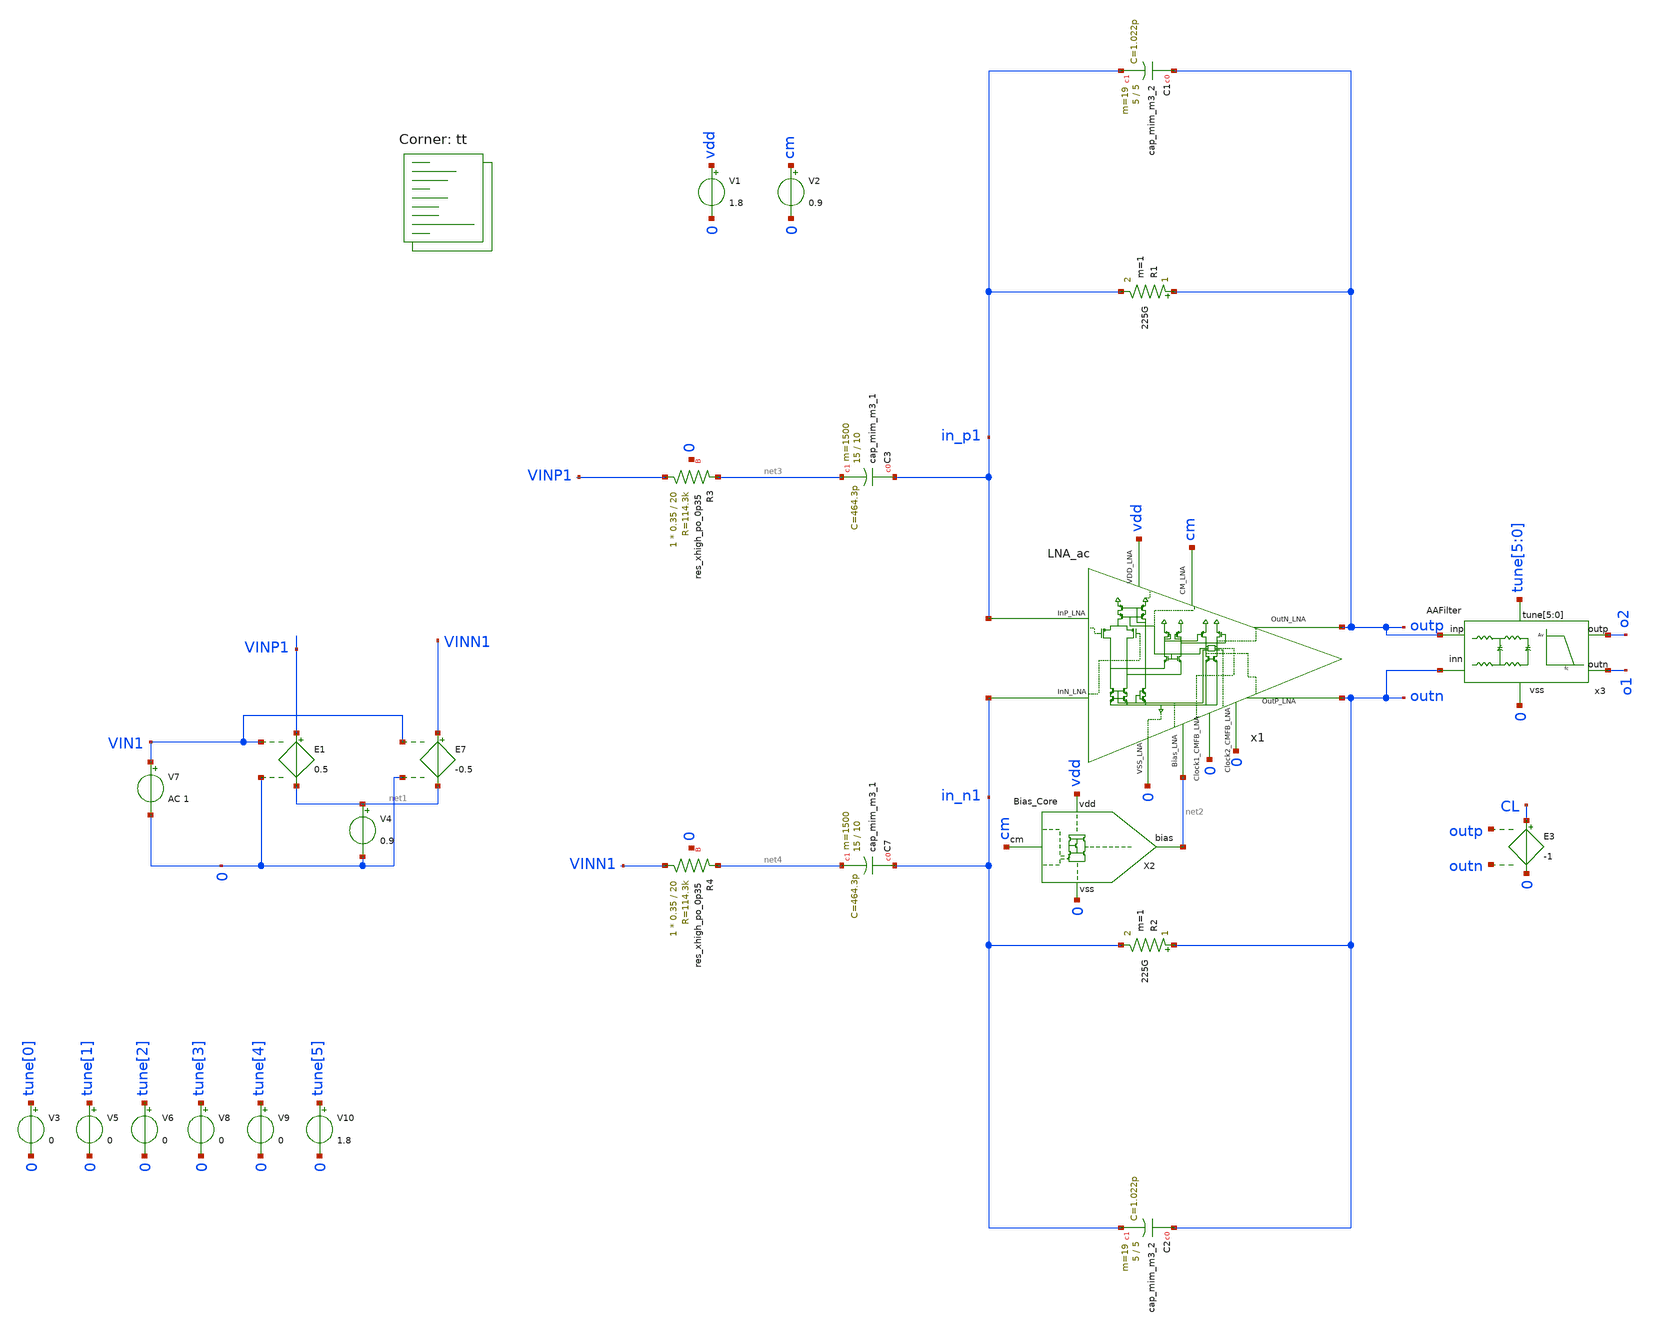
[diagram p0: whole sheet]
** sch_path: CL_ac.sch
**.subckt CL_ac
x1 in_n1 in_p1 vdd cm outp outn 0 net2 0 0 LNA_ac
V1 vdd 0 1.8
V2 cm 0 0.9
E1 VINP1 net1 VIN1 0 0.5
E7 VINN1 net1 VIN1 0 -0.5
V4 net1 0 0.9
V7 VIN1 0 AC 1
R1 outp in_p1 225G m=1
XC1 outp in_p1 sky130_fd_pr__cap_mim_m3_2 W=5 L=5 MF=19 m=19
XC2 outn in_n1 sky130_fd_pr__cap_mim_m3_2 W=5 L=5 MF=19 m=19
R2 outn in_n1 225G m=1
XR3 VINP1 net3 0 sky130_fd_pr__res_xhigh_po_0p35 L=20 mult=1 m=1
XR4 VINN1 net4 0 sky130_fd_pr__res_xhigh_po_0p35 L=20 mult=1 m=1
x3 outp outn o2 o1 0 tune[5] tune[4] tune[3] tune[2] tune[1] tune[0] AAFilter
X2 cm vdd 0 net2 Bias_Core
E3 CL 0 outp outn -1
V3 tune[0] 0 0
V5 tune[1] 0 0
V6 tune[2] 0 0
V8 tune[3] 0 0
V9 tune[4] 0 0
V10 tune[5] 0 1.8
XC7 in_n1 net4 sky130_fd_pr__cap_mim_m3_1 W=15 L=10 MF=1500 m=1500
XC3 in_p1 net3 sky130_fd_pr__cap_mim_m3_1 W=15 L=10 MF=1500 m=1500
**** begin user architecture code
.lib $::SKYWATER_MODELS/sky130.lib.spice tt


.options savecurrents gmin=1e-13
*ic v(VM5)=0.9 v(VM6)=0.9
.control


save all

save @m.xm11.msky130_fd_pr__pfet_01v8_lvt[id]
save @m.xm11.msky130_fd_pr__pfet_01v8_lvt[vgs]


*nmos
save @m.xm3.msky130_fd_pr__nfet_01v8_lvt[vgs]
save @m.xm3.msky130_fd_pr__nfet_01v8_lvt[vth]
save @m.xm3.msky130_fd_pr__nfet_01v8_lvt[vds]

save @m.xm6.msky130_fd_pr__nfet_01v8_lvt[vgs]
save @m.xm6.msky130_fd_pr__nfet_01v8_lvt[vth]
save @m.xm6.msky130_fd_pr__nfet_01v8_lvt[vds]

save @m.xm8.msky130_fd_pr__nfet_01v8_lvt[vgs]
save @m.xm8.msky130_fd_pr__nfet_01v8_lvt[vth]
save @m.xm8.msky130_fd_pr__nfet_01v8_lvt[vds]

save @m.xm9.msky130_fd_pr__nfet_01v8_lvt[vgs]
save @m.xm9.msky130_fd_pr__nfet_01v8_lvt[vth]
save @m.xm9.msky130_fd_pr__nfet_01v8_lvt[vds]

save @m.xm18.msky130_fd_pr__nfet_01v8_lvt[vgs]
save @m.xm18.msky130_fd_pr__nfet_01v8_lvt[vth]
save @m.xm18.msky130_fd_pr__nfet_01v8_lvt[vds]

save @m.xm19.msky130_fd_pr__nfet_01v8_lvt[vgs]
save @m.xm19.msky130_fd_pr__nfet_01v8_lvt[vth]
save @m.xm19.msky130_fd_pr__nfet_01v8_lvt[vds]

save @m.xm25.msky130_fd_pr__nfet_01v8_lvt[vgs]
save @m.xm25.msky130_fd_pr__nfet_01v8_lvt[vth]
save @m.xm25.msky130_fd_pr__nfet_01v8_lvt[vds]

*pmos

save @m.xm1.msky130_fd_pr__pfet_01v8_lvt[vgs]
save @m.xm1.msky130_fd_pr__pfet_01v8_lvt[vth]
save @m.xm1.msky130_fd_pr__pfet_01v8_lvt[vds]


save @m.xm2.msky130_fd_pr__pfet_01v8_lvt[vgs]
save @m.xm2.msky130_fd_pr__pfet_01v8_lvt[vth]
save @m.xm2.msky130_fd_pr__pfet_01v8_lvt[vds]


save @m.xm10.msky130_fd_pr__pfet_01v8_lvt[vgs]
save @m.xm10.msky130_fd_pr__pfet_01v8_lvt[vth]
save @m.xm10.msky130_fd_pr__pfet_01v8_lvt[vds]

save @m.xm13.msky130_fd_pr__pfet_01v8_lvt[vgs]
save @m.xm13.msky130_fd_pr__pfet_01v8_lvt[vth]
save @m.xm13.msky130_fd_pr__pfet_01v8_lvt[vds]

save @m.xm4.msky130_fd_pr__pfet_01v8_lvt[vgs]
save @m.xm4.msky130_fd_pr__pfet_01v8_lvt[vth]
save @m.xm4.msky130_fd_pr__pfet_01v8_lvt[vds]

save @m.xm5.msky130_fd_pr__pfet_01v8_lvt[vgs]
save @m.xm5.msky130_fd_pr__pfet_01v8_lvt[vth]
save @m.xm5.msky130_fd_pr__pfet_01v8_lvt[vds]

save @m.xm16.msky130_fd_pr__pfet_01v8_lvt[vgs]
save @m.xm16.msky130_fd_pr__pfet_01v8_lvt[vth]
save @m.xm16.msky130_fd_pr__pfet_01v8_lvt[vds]

save @m.xm17.msky130_fd_pr__pfet_01v8_lvt[vgs]
save @m.xm17.msky130_fd_pr__pfet_01v8_lvt[vth]
save @m.xm17.msky130_fd_pr__pfet_01v8_lvt[vds]

save @m.xm3.msky130_fd_pr__pfet_01v8_lvt[vgs]
save @m.xm3.msky130_fd_pr__pfet_01v8_lvt[vth]
save @m.xm3.msky130_fd_pr__pfet_01v8_lvt[vds]

save @m.xm20.msky130_fd_pr__pfet_01v8_lvt[vgs]
save @m.xm20.msky130_fd_pr__pfet_01v8_lvt[vth]
save @m.xm20.msky130_fd_pr__pfet_01v8_lvt[vds]

save @m.xm2.msky130_fd_pr__pfet_01v8_lvt[vgs]
save @m.xm2.msky130_fd_pr__pfet_01v8_lvt[vth]
save @m.xm2.msky130_fd_pr__pfet_01v8_lvt[vds]

save @m.xm21.msky130_fd_pr__pfet_01v8_lvt[vgs]
save @m.xm21.msky130_fd_pr__pfet_01v8_lvt[vth]
save @m.xm21.msky130_fd_pr__pfet_01v8_lvt[vds]

save @m.xm7.msky130_fd_pr__nfet_01v8_lvt[vth]

save @m.xm1.msky130_fd_pr__pfet_01v8[vgs]

save @m.xm1.msky130_fd_pr__nfet_01v8_lvt[gm]


save @m.xm1.msky130_fd_pr__nfet_01v8_lvt[gds]
save @m.xm2.msky130_fd_pr__pfet_01v8_lvt[gm]

save @m.xm23.msky130_fd_pr__nfet_01v8[cgs]
save @m.xm4.msky130_fd_pr__pfet_01v8[cgs]
save @m.xm2.msky130_fd_pr__pfet_01v8_lvt[cgs]



save @m.xm2.msky130_fd_pr__pfet_01v8_lvt[gds]


op
write CL_ac.raw
*set appendwrite


.endc
.control



*tran 50u 1500m
*save all
*plot v(Outp)-v(outn)


noise V(Outp,Outn) V7 dec 100 0.1 128
print inoise_total onoise_total
setplot noise1
plot inoise_spectrum

ac dec 10 0.1 10k
let gaind=(v(outp)-v(outn))/(v(VINP1)-v(VINN1))
let lg=vr/VIN1
let BG=(OL/CL)-1
let phase=180*cph(BG)/pi
plot db(gaind)
plot db(BG) phase


.endc






.include $::SKYWATER_STDCELLS/sky130_fd_sc_hd.spice

**** end user architecture code
**.ends

* expanding   symbol:  LNA/LNA_ac.sym # of pins=10
** sym_path: LNA_ac.sym
** sch_path: LNA_ac.sch
.subckt LNA_ac InN_LNA InP_LNA VDD_LNA CM_LNA OutN_LNA OutP_LNA VSS_LNA Bias_LNA Clock1_CMFB_LNA
+ Clock2_CMFB_LNA
*.iopin InP_LNA
*.iopin InN_LNA
*.iopin VSS_LNA
*.iopin VDD_LNA
*.iopin CM_LNA
*.opin OutP_LNA
*.opin OutN_LNA
*.iopin Clock2_CMFB_LNA
*.iopin Bias_LNA
*.iopin Clock1_CMFB_LNA
XM4 net4 InP_LNA VT2 VT2 sky130_fd_pr__pfet_01v8_lvt L=10 W=90 nf=1 ad='int((nf+1)/2) * W/nf * 0.29'
+ as='int((nf+2)/2) * W/nf * 0.29' pd='2*int((nf+1)/2) * (W/nf + 0.29)' ps='2*int((nf+2)/2) * (W/nf + 0.29)'
+ nrd='0.29 / W' nrs='0.29 / W' sa=0 sb=0 sd=0 mult=5 m=5
XM5 net3 InN_LNA VT2 VT2 sky130_fd_pr__pfet_01v8_lvt L=10 W=90 nf=1 ad='int((nf+1)/2) * W/nf * 0.29'
+ as='int((nf+2)/2) * W/nf * 0.29' pd='2*int((nf+1)/2) * (W/nf + 0.29)' ps='2*int((nf+2)/2) * (W/nf + 0.29)'
+ nrd='0.29 / W' nrs='0.29 / W' sa=0 sb=0 sd=0 mult=5 m=5
XM8 net8 Bias_LNA VSS_LNA VSS_LNA sky130_fd_pr__nfet_01v8_lvt L=20 W=10 nf=1 ad='int((nf+1)/2) * W/nf * 0.29'
+ as='int((nf+2)/2) * W/nf * 0.29' pd='2*int((nf+1)/2) * (W/nf + 0.29)' ps='2*int((nf+2)/2) * (W/nf + 0.29)'
+ nrd='0.29 / W' nrs='0.29 / W' sa=0 sb=0 sd=0 mult=3 m=3
XM9 net9 Bias_LNA VSS_LNA VSS_LNA sky130_fd_pr__nfet_01v8_lvt L=20 W=10 nf=1 ad='int((nf+1)/2) * W/nf * 0.29'
+ as='int((nf+2)/2) * W/nf * 0.29' pd='2*int((nf+1)/2) * (W/nf + 0.29)' ps='2*int((nf+2)/2) * (W/nf + 0.29)'
+ nrd='0.29 / W' nrs='0.29 / W' sa=0 sb=0 sd=0 mult=3 m=3
XM16 net7 b VDD_LNA VDD_LNA sky130_fd_pr__pfet_01v8_lvt L=20 W=6 nf=1 ad='int((nf+1)/2) * W/nf * 0.29'
+ as='int((nf+2)/2) * W/nf * 0.29' pd='2*int((nf+1)/2) * (W/nf + 0.29)' ps='2*int((nf+2)/2) * (W/nf + 0.29)'
+ nrd='0.29 / W' nrs='0.29 / W' sa=0 sb=0 sd=0 mult=1 m=1
XM17 net6 a VDD_LNA VDD_LNA sky130_fd_pr__pfet_01v8_lvt L=20 W=6 nf=1 ad='int((nf+1)/2) * W/nf * 0.29'
+ as='int((nf+2)/2) * W/nf * 0.29' pd='2*int((nf+1)/2) * (W/nf + 0.29)' ps='2*int((nf+2)/2) * (W/nf + 0.29)'
+ nrd='0.29 / W' nrs='0.29 / W' sa=0 sb=0 sd=0 mult=1 m=1
XM18 b CM_LNA net3 VSS_LNA sky130_fd_pr__nfet_01v8_lvt L=20 W=1 nf=1 ad='int((nf+1)/2) * W/nf * 0.29'
+ as='int((nf+2)/2) * W/nf * 0.29' pd='2*int((nf+1)/2) * (W/nf + 0.29)' ps='2*int((nf+2)/2) * (W/nf + 0.29)'
+ nrd='0.29 / W' nrs='0.29 / W' sa=0 sb=0 sd=0 mult=12 m=12
XM19 a CM_LNA net4 VSS_LNA sky130_fd_pr__nfet_01v8_lvt L=20 W=1 nf=1 ad='int((nf+1)/2) * W/nf * 0.29'
+ as='int((nf+2)/2) * W/nf * 0.29' pd='2*int((nf+1)/2) * (W/nf + 0.29)' ps='2*int((nf+2)/2) * (W/nf + 0.29)'
+ nrd='0.29 / W' nrs='0.29 / W' sa=0 sb=0 sd=0 mult=12 m=12
XM20 OutP_LNA a VDD_LNA VDD_LNA sky130_fd_pr__pfet_01v8_lvt L=20 W=6 nf=1 ad='int((nf+1)/2) * W/nf * 0.29'
+ as='int((nf+2)/2) * W/nf * 0.29' pd='2*int((nf+1)/2) * (W/nf + 0.29)' ps='2*int((nf+2)/2) * (W/nf + 0.29)'
+ nrd='0.29 / W' nrs='0.29 / W' sa=0 sb=0 sd=0 mult=10 m=10
XM21 OutN_LNA b VDD_LNA VDD_LNA sky130_fd_pr__pfet_01v8_lvt L=20 W=6 nf=1 ad='int((nf+1)/2) * W/nf * 0.29'
+ as='int((nf+2)/2) * W/nf * 0.29' pd='2*int((nf+1)/2) * (W/nf + 0.29)' ps='2*int((nf+2)/2) * (W/nf + 0.29)'
+ nrd='0.29 / W' nrs='0.29 / W' sa=0 sb=0 sd=0 mult=10 m=10
XM23 OutN_LNA net5 VSS_LNA VSS_LNA sky130_fd_pr__nfet_01v8_lvt L=20 W=10 nf=1 ad='int((nf+1)/2) * W/nf * 0.29'
+ as='int((nf+2)/2) * W/nf * 0.29' pd='2*int((nf+1)/2) * (W/nf + 0.29)' ps='2*int((nf+2)/2) * (W/nf + 0.29)'
+ nrd='0.29 / W' nrs='0.29 / W' sa=0 sb=0 sd=0 mult=10 m=10
XM25 OutP_LNA net5 VSS_LNA VSS_LNA sky130_fd_pr__nfet_01v8_lvt L=20 W=10 nf=1 ad='int((nf+1)/2) * W/nf * 0.29'
+ as='int((nf+2)/2) * W/nf * 0.29' pd='2*int((nf+1)/2) * (W/nf + 0.29)' ps='2*int((nf+2)/2) * (W/nf + 0.29)'
+ nrd='0.29 / W' nrs='0.29 / W' sa=0 sb=0 sd=0 mult=10 m=10
XM2 net10 net1 VDD_LNA VDD_LNA sky130_fd_pr__pfet_01v8_lvt L=20 W=2 nf=1 ad='int((nf+1)/2) * W/nf * 0.29'
+ as='int((nf+2)/2) * W/nf * 0.29' pd='2*int((nf+1)/2) * (W/nf + 0.29)' ps='2*int((nf+2)/2) * (W/nf + 0.29)'
+ nrd='0.29 / W' nrs='0.29 / W' sa=0 sb=0 sd=0 mult=4 m=4
XM3 net11 net1 VDD_LNA VDD_LNA sky130_fd_pr__pfet_01v8_lvt L=20 W=2 nf=1 ad='int((nf+1)/2) * W/nf * 0.29'
+ as='int((nf+2)/2) * W/nf * 0.29' pd='2*int((nf+1)/2) * (W/nf + 0.29)' ps='2*int((nf+2)/2) * (W/nf + 0.29)'
+ nrd='0.29 / W' nrs='0.29 / W' sa=0 sb=0 sd=0 mult=1 m=1
XM6 net2 Bias_LNA VSS_LNA VSS_LNA sky130_fd_pr__nfet_01v8_lvt L=20 W=10 nf=1 ad='int((nf+1)/2) * W/nf * 0.29'
+ as='int((nf+2)/2) * W/nf * 0.29' pd='2*int((nf+1)/2) * (W/nf + 0.29)' ps='2*int((nf+2)/2) * (W/nf + 0.29)'
+ nrd='0.29 / W' nrs='0.29 / W' sa=0 sb=0 sd=0 mult=1 m=1
E3 f1 VSS_LNA OutN_LNA VSS_LNA -1
E4 f2 VSS_LNA OutP_LNA f1 1
E5 f3 VSS_LNA f2 VSS_LNA 0.5
E6 net5 VSS_LNA CM_LNA f3 {-1000}
XC1 OutP_LNA a sky130_fd_pr__cap_mim_m3_2 W=12 L=10 MF=32 m=32
XC2 OutN_LNA b sky130_fd_pr__cap_mim_m3_2 W=12 L=10 MF=32 m=32
XM1 net4 CM_LNA net8 VSS_LNA sky130_fd_pr__nfet_01v8_lvt L=1 W=10 nf=1 ad='int((nf+1)/2) * W/nf * 0.29'
+ as='int((nf+2)/2) * W/nf * 0.29' pd='2*int((nf+1)/2) * (W/nf + 0.29)' ps='2*int((nf+2)/2) * (W/nf + 0.29)'
+ nrd='0.29 / W' nrs='0.29 / W' sa=0 sb=0 sd=0 mult=120 m=120
XM7 net3 CM_LNA net9 VSS_LNA sky130_fd_pr__nfet_01v8_lvt L=1 W=10 nf=1 ad='int((nf+1)/2) * W/nf * 0.29'
+ as='int((nf+2)/2) * W/nf * 0.29' pd='2*int((nf+1)/2) * (W/nf + 0.29)' ps='2*int((nf+2)/2) * (W/nf + 0.29)'
+ nrd='0.29 / W' nrs='0.29 / W' sa=0 sb=0 sd=0 mult=120 m=120
XM10 net1 CM_LNA net2 VSS_LNA sky130_fd_pr__nfet_01v8_lvt L=1 W=10 nf=1 ad='int((nf+1)/2) * W/nf * 0.29'
+ as='int((nf+2)/2) * W/nf * 0.29' pd='2*int((nf+1)/2) * (W/nf + 0.29)' ps='2*int((nf+2)/2) * (W/nf + 0.29)'
+ nrd='0.29 / W' nrs='0.29 / W' sa=0 sb=0 sd=0 mult=40 m=40
XM11 net1 CM_LNA net11 VDD_LNA sky130_fd_pr__pfet_01v8_lvt L=20 W=2 nf=1 ad='int((nf+1)/2) * W/nf * 0.29'
+ as='int((nf+2)/2) * W/nf * 0.29' pd='2*int((nf+1)/2) * (W/nf + 0.29)' ps='2*int((nf+2)/2) * (W/nf + 0.29)'
+ nrd='0.29 / W' nrs='0.29 / W' sa=0 sb=0 sd=0 mult=50 m=50
XM12 VT2 CM_LNA net10 VDD_LNA sky130_fd_pr__pfet_01v8_lvt L=20 W=2 nf=1 ad='int((nf+1)/2) * W/nf * 0.29'
+ as='int((nf+2)/2) * W/nf * 0.29' pd='2*int((nf+1)/2) * (W/nf + 0.29)' ps='2*int((nf+2)/2) * (W/nf + 0.29)'
+ nrd='0.29 / W' nrs='0.29 / W' sa=0 sb=0 sd=0 mult=200 m=200
XM13 b CM_LNA net7 VDD_LNA sky130_fd_pr__pfet_01v8_lvt L=20 W=6 nf=1 ad='int((nf+1)/2) * W/nf * 0.29'
+ as='int((nf+2)/2) * W/nf * 0.29' pd='2*int((nf+1)/2) * (W/nf + 0.29)' ps='2*int((nf+2)/2) * (W/nf + 0.29)'
+ nrd='0.29 / W' nrs='0.29 / W' sa=0 sb=0 sd=0 mult=10 m=10
XM14 a CM_LNA net6 VDD_LNA sky130_fd_pr__pfet_01v8_lvt L=20 W=6 nf=1 ad='int((nf+1)/2) * W/nf * 0.29'
+ as='int((nf+2)/2) * W/nf * 0.29' pd='2*int((nf+1)/2) * (W/nf + 0.29)' ps='2*int((nf+2)/2) * (W/nf + 0.29)'
+ nrd='0.29 / W' nrs='0.29 / W' sa=0 sb=0 sd=0 mult=10 m=10
.ends


* expanding   symbol:  LNA/AAFilter.sym # of pins=6
** sym_path: AAFilter.sym
** sch_path: AAFilter.sch
.subckt AAFilter inp inn outp outn vss tune[5] tune[4] tune[3] tune[2] tune[1] tune[0]
*.iopin inp
*.iopin inn
*.iopin vss
*.opin outp
*.opin outn
*.iopin tune[5],tune[4],tune[3],tune[2],tune[1],tune[0]
XR4 inp net3 vss sky130_fd_pr__res_xhigh_po_0p35 L=95 mult=1 m=1
XR15 net3 net1 vss sky130_fd_pr__res_xhigh_po_0p35 L=95 mult=1 m=1
XR16 net1 net4 vss sky130_fd_pr__res_xhigh_po_0p35 L=95 mult=1 m=1
XR17 net4 outp vss sky130_fd_pr__res_xhigh_po_0p35 L=95 mult=1 m=1
XR19 net2 net5 vss sky130_fd_pr__res_xhigh_po_0p35 L=95 mult=1 m=1
XR20 net5 inn vss sky130_fd_pr__res_xhigh_po_0p35 L=95 mult=1 m=1
XR23 outn net6 vss sky130_fd_pr__res_xhigh_po_0p35 L=95 mult=1 m=1
XR24 net6 net2 vss sky130_fd_pr__res_xhigh_po_0p35 L=95 mult=1 m=1
x2 outp outn vss tune[5] tune[4] tune[3] tune[2] tune[1] tune[0] capbank
x3 net1 net2 vss tune[5] tune[4] tune[3] tune[2] tune[1] tune[0] capbank
.ends


* expanding   symbol:  LNA/Bias_Core.sym # of pins=4
** sym_path: Bias_Core.sym
** sch_path: Bias_Core.sch
.subckt Bias_Core cm vdd vss bias
*.ipin vdd
*.ipin vss
*.opin bias
*.ipin cm
XM7 net3 bias vss vss sky130_fd_pr__nfet_01v8_lvt L=20 W=10 nf=1 ad='int((nf+1)/2) * W/nf * 0.29' as='int((nf+2)/2) * W/nf * 0.29'
+ pd='2*int((nf+1)/2) * (W/nf + 0.29)' ps='2*int((nf+2)/2) * (W/nf + 0.29)' nrd='0.29 / W' nrs='0.29 / W'
+ sa=0 sb=0 sd=0 mult=1 m=1
XM10 net4 vx vr vdd sky130_fd_pr__pfet_01v8_lvt L=20 W=10 nf=1 ad='int((nf+1)/2) * W/nf * 0.29' as='int((nf+2)/2) * W/nf * 0.29'
+ pd='2*int((nf+1)/2) * (W/nf + 0.29)' ps='2*int((nf+2)/2) * (W/nf + 0.29)' nrd='0.29 / W' nrs='0.29 / W'
+ sa=0 sb=0 sd=0 mult=20 m=20
XM11 bias cm net3 vss sky130_fd_pr__nfet_01v8_lvt L=20 W=10 nf=1 ad='int((nf+1)/2) * W/nf * 0.29' as='int((nf+2)/2) * W/nf * 0.29'
+ pd='2*int((nf+1)/2) * (W/nf + 0.29)' ps='2*int((nf+2)/2) * (W/nf + 0.29)' nrd='0.29 / W' nrs='0.29 / W'
+ sa=0 sb=0 sd=0 mult=40 m=40
XM12 net2 bias vss vss sky130_fd_pr__nfet_01v8_lvt L=20 W=10 nf=1 ad='int((nf+1)/2) * W/nf * 0.29' as='int((nf+2)/2) * W/nf * 0.29'
+ pd='2*int((nf+1)/2) * (W/nf + 0.29)' ps='2*int((nf+2)/2) * (W/nf + 0.29)' nrd='0.29 / W' nrs='0.29 / W'
+ sa=0 sb=0 sd=0 mult=1 m=1
XM13 vx cm net2 vss sky130_fd_pr__nfet_01v8_lvt L=20 W=10 nf=1 ad='int((nf+1)/2) * W/nf * 0.29' as='int((nf+2)/2) * W/nf * 0.29'
+ pd='2*int((nf+1)/2) * (W/nf + 0.29)' ps='2*int((nf+2)/2) * (W/nf + 0.29)' nrd='0.29 / W' nrs='0.29 / W'
+ sa=0 sb=0 sd=0 mult=40 m=40
XM2 net8 vx net1 vdd sky130_fd_pr__pfet_01v8_lvt L=20 W=10 nf=1 ad='int((nf+1)/2) * W/nf * 0.29' as='int((nf+2)/2) * W/nf * 0.29'
+ pd='2*int((nf+1)/2) * (W/nf + 0.29)' ps='2*int((nf+2)/2) * (W/nf + 0.29)' nrd='0.29 / W' nrs='0.29 / W'
+ sa=0 sb=0 sd=0 mult=20 m=20
XM3 net1 net1 vdd vdd sky130_fd_pr__pfet_01v8_lvt L=1 W=10 nf=1 ad='int((nf+1)/2) * W/nf * 0.29' as='int((nf+2)/2) * W/nf * 0.29'
+ pd='2*int((nf+1)/2) * (W/nf + 0.29)' ps='2*int((nf+2)/2) * (W/nf + 0.29)' nrd='0.29 / W' nrs='0.29 / W'
+ sa=0 sb=0 sd=0 mult=6 m=6
XM4 net5 net5 bias vss sky130_fd_pr__nfet_01v8_lvt L=10 W=1 nf=1 ad='int((nf+1)/2) * W/nf * 0.29' as='int((nf+2)/2) * W/nf * 0.29'
+ pd='2*int((nf+1)/2) * (W/nf + 0.29)' ps='2*int((nf+2)/2) * (W/nf + 0.29)' nrd='0.29 / W' nrs='0.29 / W'
+ sa=0 sb=0 sd=0 mult=1 m=1
XM5 net6 net6 net5 vss sky130_fd_pr__nfet_01v8_lvt L=10 W=1 nf=1 ad='int((nf+1)/2) * W/nf * 0.29' as='int((nf+2)/2) * W/nf * 0.29'
+ pd='2*int((nf+1)/2) * (W/nf + 0.29)' ps='2*int((nf+2)/2) * (W/nf + 0.29)' nrd='0.29 / W' nrs='0.29 / W'
+ sa=0 sb=0 sd=0 mult=1 m=1
XM8 net7 net7 net6 vss sky130_fd_pr__nfet_01v8_lvt L=10 W=1 nf=1 ad='int((nf+1)/2) * W/nf * 0.29' as='int((nf+2)/2) * W/nf * 0.29'
+ pd='2*int((nf+1)/2) * (W/nf + 0.29)' ps='2*int((nf+2)/2) * (W/nf + 0.29)' nrd='0.29 / W' nrs='0.29 / W'
+ sa=0 sb=0 sd=0 mult=1 m=1
XM9 vx vx net7 vss sky130_fd_pr__nfet_01v8_lvt L=10 W=1 nf=1 ad='int((nf+1)/2) * W/nf * 0.29' as='int((nf+2)/2) * W/nf * 0.29'
+ pd='2*int((nf+1)/2) * (W/nf + 0.29)' ps='2*int((nf+2)/2) * (W/nf + 0.29)' nrd='0.29 / W' nrs='0.29 / W'
+ sa=0 sb=0 sd=0 mult=1 m=1
XM23 bias vx net4 vdd sky130_fd_pr__pfet_01v8_lvt L=20 W=10 nf=1 ad='int((nf+1)/2) * W/nf * 0.29' as='int((nf+2)/2) * W/nf * 0.29'
+ pd='2*int((nf+1)/2) * (W/nf + 0.29)' ps='2*int((nf+2)/2) * (W/nf + 0.29)' nrd='0.29 / W' nrs='0.29 / W'
+ sa=0 sb=0 sd=0 mult=5 m=5
XM24 vx vx net8 vdd sky130_fd_pr__pfet_01v8_lvt L=20 W=10 nf=1 ad='int((nf+1)/2) * W/nf * 0.29' as='int((nf+2)/2) * W/nf * 0.29'
+ pd='2*int((nf+1)/2) * (W/nf + 0.29)' ps='2*int((nf+2)/2) * (W/nf + 0.29)' nrd='0.29 / W' nrs='0.29 / W'
+ sa=0 sb=0 sd=0 mult=5 m=5
R27 vdd vr 3e6 m=1
.ends


* expanding   symbol:  LNA/capbank.sym # of pins=4
** sym_path: capbank.sym
** sch_path: capbank.sch
.subckt capbank vp_cap vn_cap vss_cap tune[5] tune[4] tune[3] tune[2] tune[1] tune[0]
*.iopin vp_cap
*.iopin vn_cap
*.ipin tune[5],tune[4],tune[3],tune[2],tune[1],tune[0]
*.ipin vss_cap
x6 tune[5] net1 net2 vss_cap cap_sw
XC11 net2 vp_cap sky130_fd_pr__cap_mim_m3_1 W=5 L=5.5 MF=160 m=160
XC12 net1 vn_cap sky130_fd_pr__cap_mim_m3_1 W=5 L=5.5 MF=160 m=160
XC21 vn_cap net1 sky130_fd_pr__cap_mim_m3_1 W=5 L=5.5 MF=160 m=160
XC22 vp_cap net2 sky130_fd_pr__cap_mim_m3_1 W=5 L=5.5 MF=160 m=160
x1 tune[4] net3 net4 vss_cap cap_sw
XC1 net4 vp_cap sky130_fd_pr__cap_mim_m3_1 W=5 L=5.5 MF=80 m=80
XC2 net3 vn_cap sky130_fd_pr__cap_mim_m3_1 W=5 L=5.5 MF=80 m=80
XC3 vn_cap net3 sky130_fd_pr__cap_mim_m3_1 W=5 L=5.5 MF=80 m=80
XC4 vp_cap net4 sky130_fd_pr__cap_mim_m3_1 W=5 L=5.5 MF=80 m=80
x2 tune[3] net5 net6 vss_cap cap_sw
XC5 net6 vp_cap sky130_fd_pr__cap_mim_m3_1 W=5 L=5.5 MF=40 m=40
XC6 net5 vn_cap sky130_fd_pr__cap_mim_m3_1 W=5 L=5.5 MF=40 m=40
XC7 vn_cap net5 sky130_fd_pr__cap_mim_m3_1 W=5 L=5.5 MF=40 m=40
XC8 vp_cap net6 sky130_fd_pr__cap_mim_m3_1 W=5 L=5.5 MF=40 m=40
x3 tune[2] net7 net8 vss_cap cap_sw
XC9 net8 vp_cap sky130_fd_pr__cap_mim_m3_1 W=5 L=5.5 MF=20 m=20
XC10 net7 vn_cap sky130_fd_pr__cap_mim_m3_1 W=5 L=5.5 MF=20 m=20
XC13 vn_cap net7 sky130_fd_pr__cap_mim_m3_1 W=5 L=5.5 MF=20 m=20
XC14 vp_cap net8 sky130_fd_pr__cap_mim_m3_1 W=5 L=5.5 MF=20 m=20
x4 tune[1] net9 net10 vss_cap cap_sw
XC15 net10 vp_cap sky130_fd_pr__cap_mim_m3_1 W=5 L=5.5 MF=10 m=10
XC16 net9 vn_cap sky130_fd_pr__cap_mim_m3_1 W=5 L=5.5 MF=10 m=10
XC17 vn_cap net9 sky130_fd_pr__cap_mim_m3_1 W=5 L=5.5 MF=10 m=10
XC18 vp_cap net10 sky130_fd_pr__cap_mim_m3_1 W=5 L=5.5 MF=10 m=10
x5 tune[0] net11 net12 vss_cap cap_sw
XC19 vp_cap net12 sky130_fd_pr__cap_mim_m3_1 W=5 L=5.5 MF=5 m=5
XC20 vn_cap net11 sky130_fd_pr__cap_mim_m3_1 W=5 L=5.5 MF=5 m=5
XC23 vn_cap net11 sky130_fd_pr__cap_mim_m3_1 W=5 L=5.5 MF=5 m=5
XC24 vp_cap net12 sky130_fd_pr__cap_mim_m3_1 W=5 L=5.5 MF=5 m=5
.ends


* expanding   symbol:  LNA/cap_sw.sym # of pins=4
** sym_path: cap_sw.sym
** sch_path: cap_sw.sch
.subckt cap_sw en_sw vn_sw vp_sw vss_sw
*.ipin en_sw
*.ipin vss_sw
*.opin vn_sw
*.opin vp_sw
XM15 vp_sw en_sw vn_sw vss_sw sky130_fd_pr__nfet_01v8 L=0.15 W='5 * 13 ' nf=13 ad='int((nf+1)/2) * W / nf * 0.29'
+ as='int((nf+2)/2) * W / nf * 0.29' pd='2*int((nf+1)/2) * (W / nf + 0.29)' ps='2*int((nf+2)/2) * (W / nf + 0.29)'
+ nrd='0.29 / W ' nrs='0.29 / W ' sa=0 sb=0 sd=0 mult=1 m=1
XM5 vn_sw en_sw vss_sw vss_sw sky130_fd_pr__nfet_01v8 L=0.15 W='5 * 1 ' nf=1 ad='int((nf+1)/2) * W / nf * 0.29'
+ as='int((nf+2)/2) * W / nf * 0.29' pd='2*int((nf+1)/2) * (W / nf + 0.29)' ps='2*int((nf+2)/2) * (W / nf + 0.29)'
+ nrd='0.29 / W ' nrs='0.29 / W ' sa=0 sb=0 sd=0 mult=1 m=1
XM7 vp_sw en_sw vss_sw vss_sw sky130_fd_pr__nfet_01v8 L=0.15 W='5 * 1 ' nf=1 ad='int((nf+1)/2) * W / nf * 0.29'
+ as='int((nf+2)/2) * W / nf * 0.29' pd='2*int((nf+1)/2) * (W / nf + 0.29)' ps='2*int((nf+2)/2) * (W / nf + 0.29)'
+ nrd='0.29 / W ' nrs='0.29 / W ' sa=0 sb=0 sd=0 mult=1 m=1
XM1 vss_sw vss_sw vss_sw vss_sw sky130_fd_pr__nfet_01v8 L=0.15 W='5 * 2 ' nf=2 ad='int((nf+1)/2) * W / nf * 0.29'
+ as='int((nf+2)/2) * W / nf * 0.29' pd='2*int((nf+1)/2) * (W / nf + 0.29)' ps='2*int((nf+2)/2) * (W / nf + 0.29)'
+ nrd='0.29 / W ' nrs='0.29 / W ' sa=0 sb=0 sd=0 mult=1 m=1
.ends

.end
